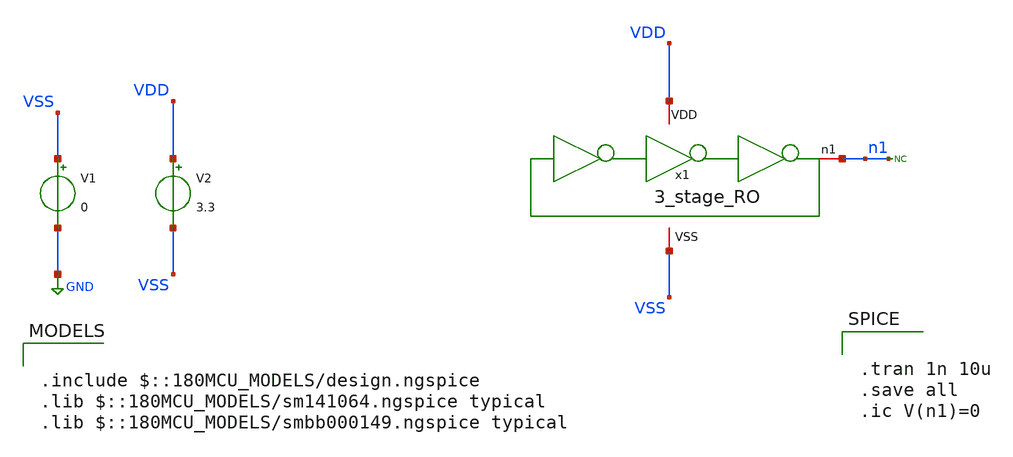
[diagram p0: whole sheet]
** sch_path: gf180_examples/inverter/xschem/3_stage_RO_tb_tran.sch
**.subckt 3_stage_RO_tb_tran
x1 VDD VSS n1 3_stage_RO
V1 VSS GND 0
V2 VDD VSS 3.3
* noconn n1
**** begin user architecture code

.include $::180MCU_MODELS/design.ngspice
.lib $::180MCU_MODELS/sm141064.ngspice typical
.lib $::180MCU_MODELS/smbb000149.ngspice typical



.tran 1n 10u
.save all
.ic V(n1)=0


**** end user architecture code
**.ends

* expanding   symbol:  Chipathon2025_gf180/gf180_examples/inverter/xschem/3_stage_RO.sym # of pins=3
** sym_path: Chipathon2025_gf180/gf180_examples/inverter/xschem/3_stage_RO.sym
** sch_path: Chipathon2025_gf180/gf180_examples/inverter/xschem/3_stage_RO.sch
.subckt 3_stage_RO VDD VSS n1
*.iopin VDD
*.iopin VSS
*.iopin n1
x1 n1 VDD VSS n2 inverter
x2 n2 VDD VSS n3 inverter
x3 n3 VDD VSS n1 inverter
C1 n2 VSS 100f m=1
C2 n3 VSS 100f m=1
C3 n1 VSS 100f m=1
.ends

.GLOBAL GND
.end
